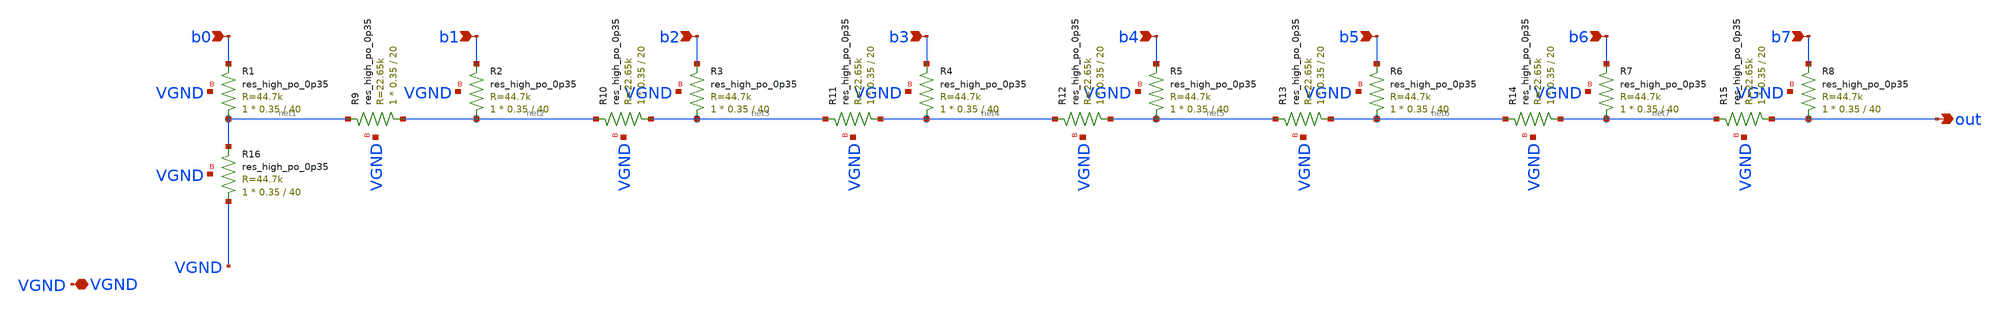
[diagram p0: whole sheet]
** sch_path: xschem/r2r.sch
**.subckt r2r b0 b1 b2 b3 b4 b5 b6 b7 out VGND
*.ipin b0
*.ipin b1
*.ipin b2
*.ipin b3
*.ipin b4
*.ipin b5
*.ipin b6
*.ipin b7
*.opin out
*.iopin VGND
XR1 net1 b0 VGND sky130_fd_pr__res_high_po_0p35 L=40 mult=1 m=1
XR2 net2 b1 VGND sky130_fd_pr__res_high_po_0p35 L=40 mult=1 m=1
XR3 net3 b2 VGND sky130_fd_pr__res_high_po_0p35 L=40 mult=1 m=1
XR4 net4 b3 VGND sky130_fd_pr__res_high_po_0p35 L=40 mult=1 m=1
XR5 net5 b4 VGND sky130_fd_pr__res_high_po_0p35 L=40 mult=1 m=1
XR6 net6 b5 VGND sky130_fd_pr__res_high_po_0p35 L=40 mult=1 m=1
XR7 net7 b6 VGND sky130_fd_pr__res_high_po_0p35 L=40 mult=1 m=1
XR8 out b7 VGND sky130_fd_pr__res_high_po_0p35 L=40 mult=1 m=1
XR9 net2 net1 VGND sky130_fd_pr__res_high_po_0p35 L=20 mult=1 m=1
XR10 net3 net2 VGND sky130_fd_pr__res_high_po_0p35 L=20 mult=1 m=1
XR11 net4 net3 VGND sky130_fd_pr__res_high_po_0p35 L=20 mult=1 m=1
XR12 net5 net4 VGND sky130_fd_pr__res_high_po_0p35 L=20 mult=1 m=1
XR13 net6 net5 VGND sky130_fd_pr__res_high_po_0p35 L=20 mult=1 m=1
XR14 net7 net6 VGND sky130_fd_pr__res_high_po_0p35 L=20 mult=1 m=1
XR15 out net7 VGND sky130_fd_pr__res_high_po_0p35 L=20 mult=1 m=1
XR16 VGND net1 VGND sky130_fd_pr__res_high_po_0p35 L=40 mult=1 m=1
**.ends
.end
